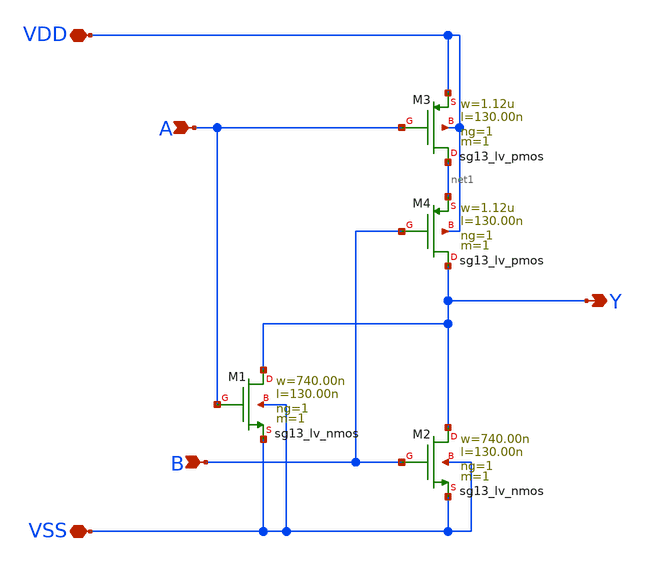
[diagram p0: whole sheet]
** sch_path: ihp-sg13g2/libs.tech/xschem/sg13g2_stdcells/sg13g2_nor2_1.sch
* Copyright 2023 IHP PDK Authors
* Licensed under the Apache License, Version 2.0 (the "License");
* you may not use this file except in compliance with the License.
* You may obtain a copy of the License at
* https://www.apache.org/licenses/LICENSE-2.0
* Unless required by applicable law or agreed to in writing, software
* distributed under the License is distributed on an "AS IS" BASIS,
* WITHOUT WARRANTIES OR CONDITIONS OF ANY KIND, either express or implied.
* See the License for the specific language governing permissions and
* limitations under the License.
**.subckt sg13g2_nor2_1 Y B A VDD VSS
*.opin Y
*.ipin B
*.ipin A
*.iopin VDD
*.iopin VSS
XM1 Y A VSS VSS sg13_lv_nmos w=740.00n l=130.00n ng=1 m=1 mm_ok=1
XM2 Y B VSS VSS sg13_lv_nmos w=740.00n l=130.00n ng=1 m=1 mm_ok=1
XM3 net1 A VDD VDD sg13_lv_pmos w=1.12u l=130.00n ng=1 m=1 mm_ok=1
XM4 Y B net1 VDD sg13_lv_pmos w=1.12u l=130.00n ng=1 m=1 mm_ok=1
**.ends
.end
